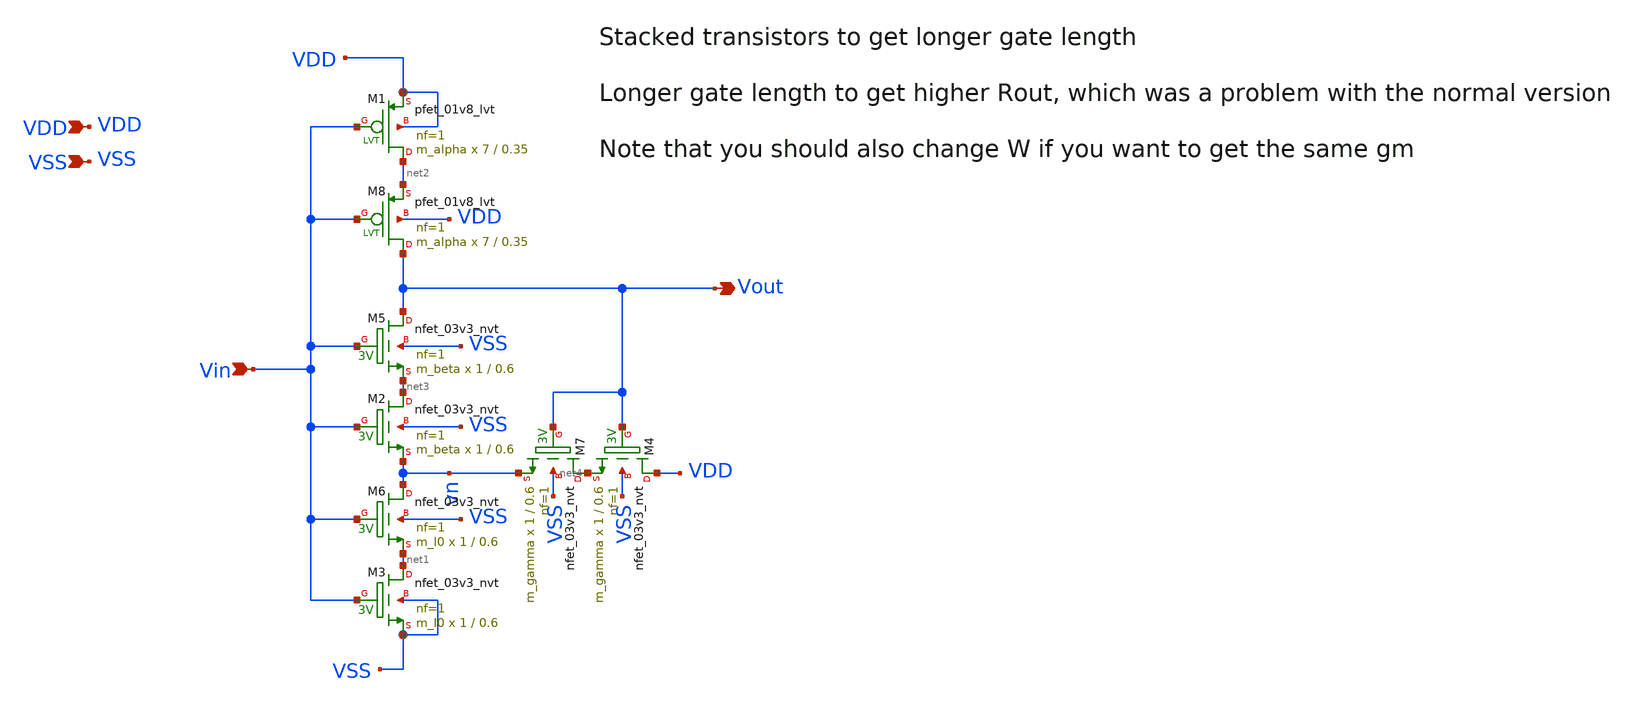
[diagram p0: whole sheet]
** sch_path: design/THESIS_EXP_RO_INVERTER_SKY130A/INV_NVT_feedback_LLL.sch
**.subckt INV_NVT_feedback_LLL VSS Vin Vout VDD
*.ipin VSS
*.ipin Vin
*.opin Vout
*.ipin VDD
XM1 net2 Vin VDD VDD sky130_fd_pr__pfet_01v8_lvt L=0.35 W=7 nf=1 ad='int((nf+1)/2) * W/nf * 0.29' as='int((nf+2)/2) * W/nf * 0.29'
+ pd='2*int((nf+1)/2) * (W/nf + 0.29)' ps='2*int((nf+2)/2) * (W/nf + 0.29)' nrd='0.29 / W' nrs='0.29 / W'
+ sa=0 sb=0 sd=0 mult=m_alpha m=m_alpha
XM2 net3 Vin vn VSS sky130_fd_pr__nfet_03v3_nvt L=0.6 W=1 nf=1 ad='int((nf+1)/2) * W/nf * 0.29' as='int((nf+2)/2) * W/nf * 0.29'
+ pd='2*int((nf+1)/2) * (W/nf + 0.29)' ps='2*int((nf+2)/2) * (W/nf + 0.29)' nrd='0.29 / W' nrs='0.29 / W'
+ sa=0 sb=0 sd=0 mult=m_beta m=m_beta
XM3 net1 Vin VSS VSS sky130_fd_pr__nfet_03v3_nvt L=0.6 W=1 nf=1 ad='int((nf+1)/2) * W/nf * 0.29' as='int((nf+2)/2) * W/nf * 0.29'
+ pd='2*int((nf+1)/2) * (W/nf + 0.29)' ps='2*int((nf+2)/2) * (W/nf + 0.29)' nrd='0.29 / W' nrs='0.29 / W'
+ sa=0 sb=0 sd=0 mult=m_I0 m=m_I0
XM4 VDD Vout net4 VSS sky130_fd_pr__nfet_03v3_nvt L=0.6 W=1 nf=1 ad='int((nf+1)/2) * W/nf * 0.29' as='int((nf+2)/2) * W/nf * 0.29'
+ pd='2*int((nf+1)/2) * (W/nf + 0.29)' ps='2*int((nf+2)/2) * (W/nf + 0.29)' nrd='0.29 / W' nrs='0.29 / W'
+ sa=0 sb=0 sd=0 mult=m_gamma m=m_gamma
XM5 Vout Vin net3 VSS sky130_fd_pr__nfet_03v3_nvt L=0.6 W=1 nf=1 ad='int((nf+1)/2) * W/nf * 0.29' as='int((nf+2)/2) * W/nf * 0.29'
+ pd='2*int((nf+1)/2) * (W/nf + 0.29)' ps='2*int((nf+2)/2) * (W/nf + 0.29)' nrd='0.29 / W' nrs='0.29 / W'
+ sa=0 sb=0 sd=0 mult=m_beta m=m_beta
XM6 vn Vin net1 VSS sky130_fd_pr__nfet_03v3_nvt L=0.6 W=1 nf=1 ad='int((nf+1)/2) * W/nf * 0.29' as='int((nf+2)/2) * W/nf * 0.29'
+ pd='2*int((nf+1)/2) * (W/nf + 0.29)' ps='2*int((nf+2)/2) * (W/nf + 0.29)' nrd='0.29 / W' nrs='0.29 / W'
+ sa=0 sb=0 sd=0 mult=m_I0 m=m_I0
XM7 net4 Vout vn VSS sky130_fd_pr__nfet_03v3_nvt L=0.6 W=1 nf=1 ad='int((nf+1)/2) * W/nf * 0.29' as='int((nf+2)/2) * W/nf * 0.29'
+ pd='2*int((nf+1)/2) * (W/nf + 0.29)' ps='2*int((nf+2)/2) * (W/nf + 0.29)' nrd='0.29 / W' nrs='0.29 / W'
+ sa=0 sb=0 sd=0 mult=m_gamma m=m_gamma
XM8 Vout Vin net2 VDD sky130_fd_pr__pfet_01v8_lvt L=0.35 W=7 nf=1 ad='int((nf+1)/2) * W/nf * 0.29' as='int((nf+2)/2) * W/nf * 0.29'
+ pd='2*int((nf+1)/2) * (W/nf + 0.29)' ps='2*int((nf+2)/2) * (W/nf + 0.29)' nrd='0.29 / W' nrs='0.29 / W'
+ sa=0 sb=0 sd=0 mult=m_alpha m=m_alpha
**.ends
.end
